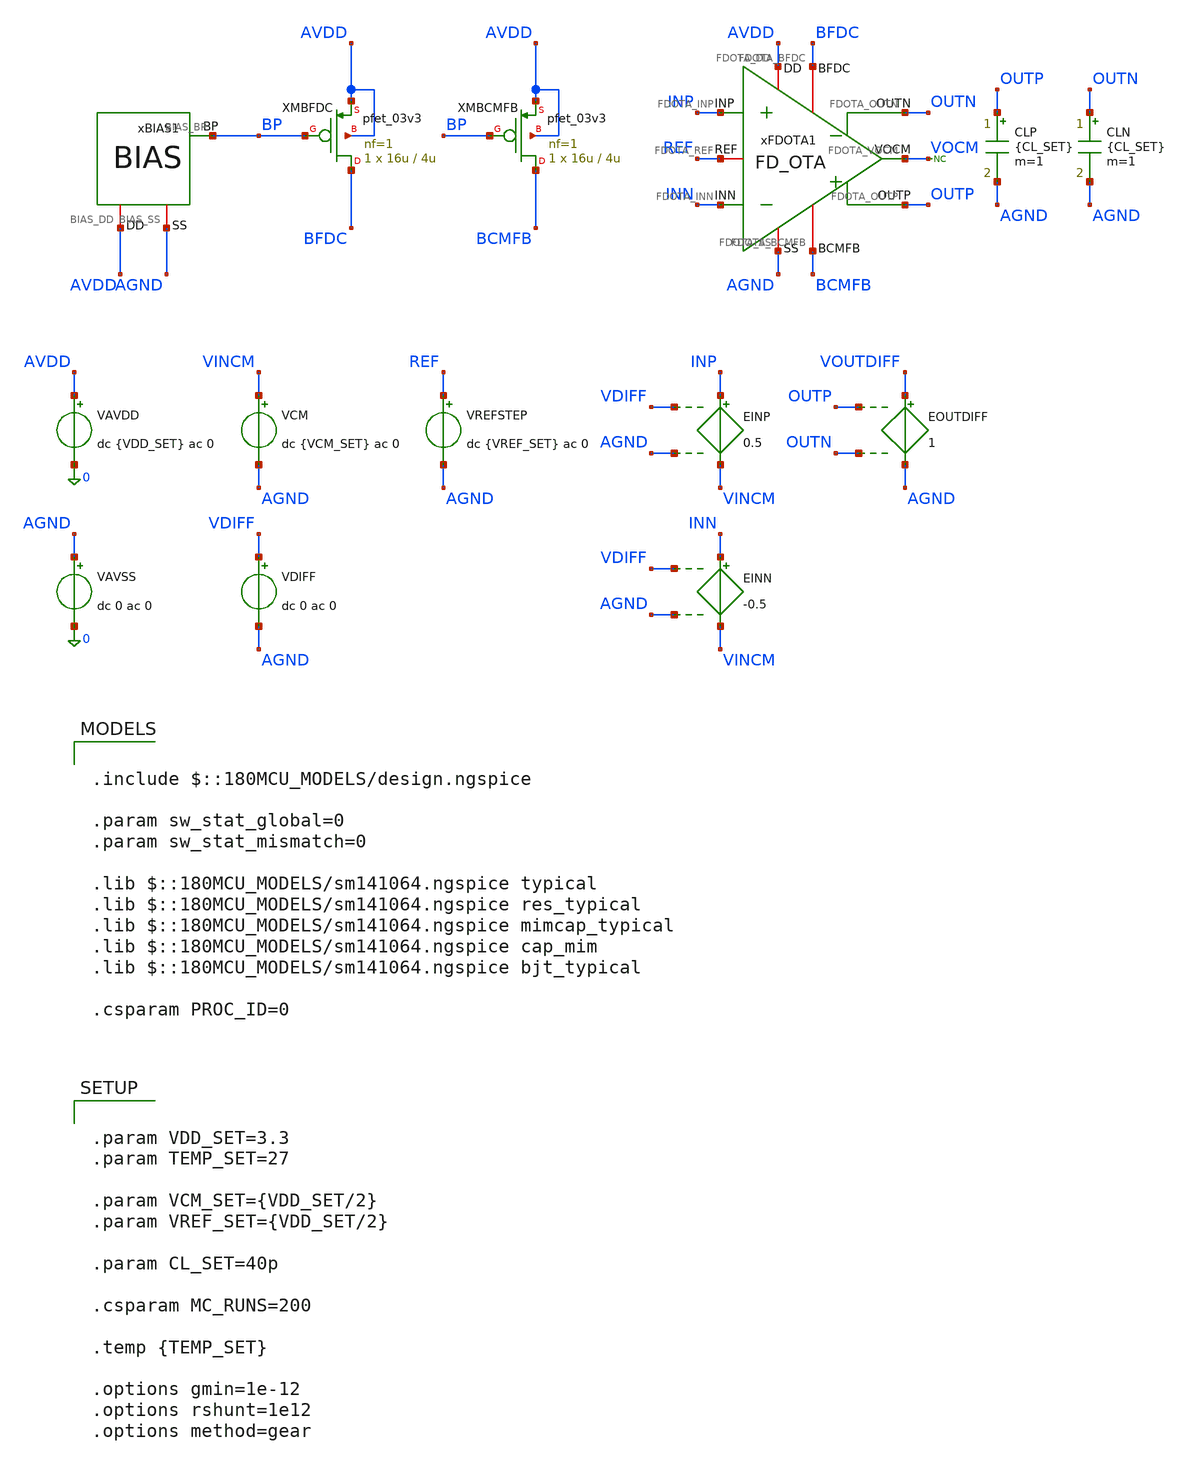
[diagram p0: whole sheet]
** sch_path: Design_Files/IC Design/Testbench/ANALOG_BLOCKS/FD_OTA/Open_Loop/FD_OTA_TB_OL_NOM.sch
**.subckt FD_OTA_TB_OL_NOM
VAVDD AVDD 0 dc {VDD_SET} ac 0
.save i(vavdd)
VCM VINCM AGND dc {VCM_SET} ac 0
VDIFF VDIFF AGND dc 0 ac 0
VAVSS AGND 0 dc 0 ac 0
VREFSTEP REF AGND dc {VREF_SET} ac 0
EINP INP VINCM VDIFF AGND 0.5
EINN INN VINCM VDIFF AGND -0.5
CLP OUTP AGND {CL_SET} m=1
CLN OUTN AGND {CL_SET} m=1
* noconn VOCM
xFDOTA1 AVDD AGND INP INN OUTN BFDC OUTP BCMFB REF VOCM FD_OTA
xBIAS1 AVDD AGND BP BIAS
XMBFDC BFDC BP AVDD AVDD pfet_03v3 L=4u W=16u nf=1 ad='int((nf+1)/2) * W/nf * 0.18u' as='int((nf+2)/2) * W/nf * 0.18u'
+ pd='2*int((nf+1)/2) * (W/nf + 0.18u)' ps='2*int((nf+2)/2) * (W/nf + 0.18u)' nrd='0.18u / W' nrs='0.18u / W'
+ sa=0 sb=0 sd=0 m=1
XMBCMFB BCMFB BP AVDD AVDD pfet_03v3 L=4u W=16u nf=1 ad='int((nf+1)/2) * W/nf * 0.18u' as='int((nf+2)/2) * W/nf * 0.18u'
+ pd='2*int((nf+1)/2) * (W/nf + 0.18u)' ps='2*int((nf+2)/2) * (W/nf + 0.18u)' nrd='0.18u / W' nrs='0.18u / W'
+ sa=0 sb=0 sd=0 m=1
EOUTDIFF VOUTDIFF AGND OUTP OUTN 1
**** begin user architecture code

.include $::180MCU_MODELS/design.ngspice

.param sw_stat_global=0
.param sw_stat_mismatch=0

.lib $::180MCU_MODELS/sm141064.ngspice typical
.lib $::180MCU_MODELS/sm141064.ngspice res_typical
.lib $::180MCU_MODELS/sm141064.ngspice mimcap_typical
.lib $::180MCU_MODELS/sm141064.ngspice cap_mim
.lib $::180MCU_MODELS/sm141064.ngspice bjt_typical

.csparam PROC_ID=0




.control

destroy all

set noaskquit
set wr_singlescale
unset wr_vecnames

option klu
option numdgt=15
option method=gear
option maxord=2
option plotwinsize=0

if $&PROC_ID = 0
set proc=NOM
else
if $&PROC_ID = 1
set proc=FF
else
if $&PROC_ID = 2
set proc=SS
else
if $&PROC_ID = 3
set proc=FS
else
set proc=SF
end
end
end
end

shell mkdir -p /foss/designs/ECG_Acquisition_IC/Measurement_Results/IC_Simulation/ANALOG_BLOCKS/FD_OTA/{$proc}.Result_txt
shell rm -f /foss/designs/ECG_Acquisition_IC/Measurement_Results/IC_Simulation/ANALOG_BLOCKS/FD_OTA/{$proc}.Result_txt/{$proc}.ol_*.txt

foreach vddval 3.3 3.0 3.6
foreach tval 27 -40 125

if $vddval = 3.3
if $tval = 27
set case=nom
else
if $tval = -40
set case=tl
else
set case=th
end
end
else
if $vddval = 3.0
if $tval = 27
set case=vl
else
if $tval = -40
set case=vltl
else
set case=vlth
end
end
else
if $tval = 27
set case=vh
else
if $tval = -40
set case=vhtl
else
set case=vhth
end
end
end
end

alterparam VDD_SET=$vddval
alterparam TEMP_SET=$tval
reset

option klu

save all
save @m.xmbfdc.m0[id]
save @m.xmbcmfb.m0[id]

* OP

op

let vdd=v(AVDD)-v(AGND)
let vinp=v(INP)-v(AGND)
let vinn=v(INN)-v(AGND)
let voutp=v(OUTP)-v(AGND)
let voutn=v(OUTN)-v(AGND)
let voutcm=0.5*(voutp+voutn)
let voutdiff=voutp-voutn
let vref=v(REF)-v(AGND)
let vocm=v(VOCM)-v(AGND)
let bfdc=v(BFDC)-v(AGND)
let bcmfb=v(BCMFB)-v(AGND)
let idd_total=abs(vavdd#branch)
let ibias_fdc=abs(@m.xmbfdc.m0[id])
let ibias_cmfb=abs(@m.xmbcmfb.m0[id])

wrdata /foss/designs/ECG_Acquisition_IC/Measurement_Results/IC_Simulation/ANALOG_BLOCKS/FD_OTA/{$proc}.Result_txt/{$proc}.ol_{$case}_op.txt
+ vdd vinp vinn voutp voutn voutcm voutdiff vref vocm bfdc bcmfb idd_total ibias_fdc ibias_cmfb

* DIFF AC

alter @VCM[ACMAG]=0
alter @VDIFF[ACMAG]=1
alter @VDIFF[ACPHASE]=0
alter @VREFSTEP[ACMAG]=0
alter @VAVDD[ACMAG]=0
alter @VAVSS[ACMAG]=0

ac dec 200 0.01 1G

let vin_diff=v(INP)-v(INN)
let vout_diff=v(OUTP)-v(OUTN)

let vin_diff_real=real(vin_diff)
let vin_diff_imag=imag(vin_diff)
let vout_diff_real=real(vout_diff)
let vout_diff_imag=imag(vout_diff)

setscale frequency

wrdata /foss/designs/ECG_Acquisition_IC/Measurement_Results/IC_Simulation/ANALOG_BLOCKS/FD_OTA/{$proc}.Result_txt/{$proc}.ol_{$case}_diff_ac.txt
+ vin_diff_real vin_diff_imag vout_diff_real vout_diff_imag

* CM AC

alter @VCM[ACMAG]=1
alter @VCM[ACPHASE]=0
alter @VDIFF[ACMAG]=0
alter @VREFSTEP[ACMAG]=0
alter @VAVDD[ACMAG]=0
alter @VAVSS[ACMAG]=0

ac dec 200 0.01 1G

let vin_cm=0.5*(v(INP)+v(INN))-v(AGND)
let vout_diff=v(OUTP)-v(OUTN)

let vin_cm_real=real(vin_cm)
let vin_cm_imag=imag(vin_cm)
let vout_diff_real=real(vout_diff)
let vout_diff_imag=imag(vout_diff)

setscale frequency

wrdata /foss/designs/ECG_Acquisition_IC/Measurement_Results/IC_Simulation/ANALOG_BLOCKS/FD_OTA/{$proc}.Result_txt/{$proc}.ol_{$case}_cm_ac.txt
+ vin_cm_real vin_cm_imag vout_diff_real vout_diff_imag

* PSRR+

alter @VCM[ACMAG]=0
alter @VDIFF[ACMAG]=0
alter @VREFSTEP[ACMAG]=0
alter @VAVDD[ACMAG]=1
alter @VAVDD[ACPHASE]=0
alter @VAVSS[ACMAG]=0

ac dec 200 0.01 1G

let vsup=v(AVDD)-v(AGND)
let vout_diff=v(OUTP)-v(OUTN)

let vsup_real=real(vsup)
let vsup_imag=imag(vsup)
let vout_diff_real=real(vout_diff)
let vout_diff_imag=imag(vout_diff)

setscale frequency

wrdata /foss/designs/ECG_Acquisition_IC/Measurement_Results/IC_Simulation/ANALOG_BLOCKS/FD_OTA/{$proc}.Result_txt/{$proc}.ol_{$case}_psrrp_ac.txt
+ vsup_real vsup_imag vout_diff_real vout_diff_imag

* PSRR-

alter @VCM[ACMAG]=0
alter @VDIFF[ACMAG]=0
alter @VREFSTEP[ACMAG]=0
alter @VAVDD[ACMAG]=0
alter @VAVSS[ACMAG]=1
alter @VAVSS[ACPHASE]=0

ac dec 200 0.01 1G

let vagnd=v(AGND)
let vout_diff=v(OUTP)-v(OUTN)

let vagnd_real=real(vagnd)
let vagnd_imag=imag(vagnd)
let vout_diff_real=real(vout_diff)
let vout_diff_imag=imag(vout_diff)

setscale frequency

wrdata /foss/designs/ECG_Acquisition_IC/Measurement_Results/IC_Simulation/ANALOG_BLOCKS/FD_OTA/{$proc}.Result_txt/{$proc}.ol_{$case}_psrrn_ac.txt
+ vagnd_real vagnd_imag vout_diff_real vout_diff_imag

* VTC

alter @VCM[ACMAG]=0
alter @VDIFF[ACMAG]=0
alter @VREFSTEP[ACMAG]=0
alter @VAVDD[ACMAG]=0
alter @VAVSS[ACMAG]=0

dc VDIFF -20m 20m 1u

let vin_cm=0.5*(v(INP)+v(INN))-v(AGND)
let vin_diff=v(INP)-v(INN)
let voutp=v(OUTP)-v(AGND)
let voutn=v(OUTN)-v(AGND)
let voutcm=0.5*(voutp+voutn)
let voutdiff=voutp-voutn
let vocm=v(VOCM)-v(AGND)
let idd_total=abs(vavdd#branch)

setscale vin_diff

wrdata /foss/designs/ECG_Acquisition_IC/Measurement_Results/IC_Simulation/ANALOG_BLOCKS/FD_OTA/{$proc}.Result_txt/{$proc}.ol_{$case}_vtc.txt
+ vin_cm v(INP) v(INN) voutp voutn voutcm voutdiff vocm idd_total

* NOISE

option sparse

alter @VCM[ACMAG]=0
alter @VDIFF[ACMAG]=1
alter @VDIFF[ACPHASE]=0
alter @VREFSTEP[ACMAG]=0
alter @VAVDD[ACMAG]=0
alter @VAVSS[ACMAG]=0

noise v(VOUTDIFF) VDIFF dec 100 0.01 1k

setplot previous
setscale frequency

wrdata /foss/designs/ECG_Acquisition_IC/Measurement_Results/IC_Simulation/ANALOG_BLOCKS/FD_OTA/{$proc}.Result_txt/{$proc}.ol_{$case}_noise.txt
+ onoise_spectrum inoise_spectrum

destroy all

end
end

quit

.endc




.param VDD_SET=3.3
.param TEMP_SET=27

.param VCM_SET={VDD_SET/2}
.param VREF_SET={VDD_SET/2}

.param CL_SET=40p

.csparam MC_RUNS=200

.temp {TEMP_SET}

.options gmin=1e-12
.options rshunt=1e12
.options method=gear


**** end user architecture code
**.ends
.end
